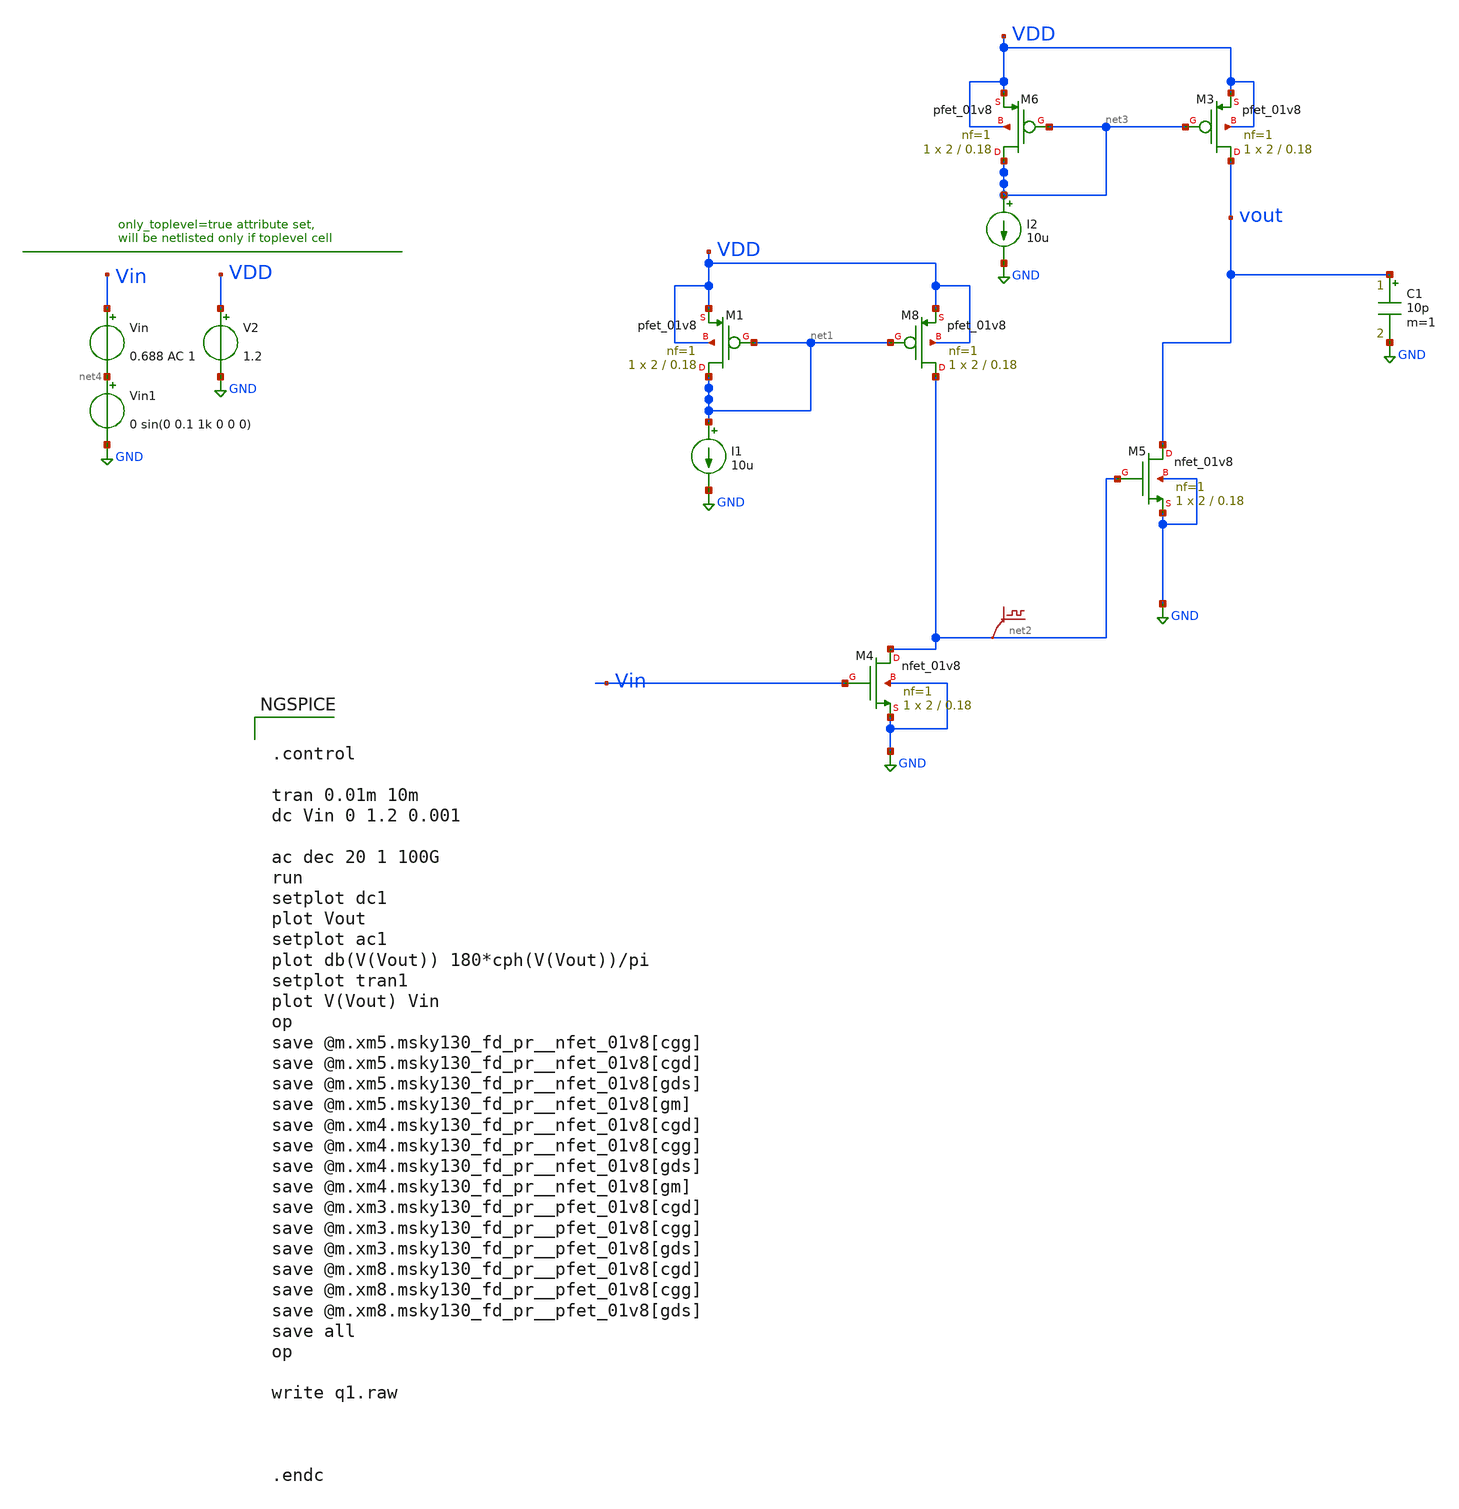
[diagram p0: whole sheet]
** sch_path: q1.sch
**.subckt q1
Vin Vin net4 0.688 AC 1
V2 VDD GND 1.2
XM4 net2 Vin GND GND sky130_fd_pr__nfet_01v8 L=0.18 W=2 nf=1 ad='int((nf+1)/2) * W/nf * 0.29' as='int((nf+2)/2) * W/nf * 0.29'
+ pd='2*int((nf+1)/2) * (W/nf + 0.29)' ps='2*int((nf+2)/2) * (W/nf + 0.29)' nrd='0.29 / W' nrs='0.29 / W'
+ sa=0 sb=0 sd=0 mult=1 m=1
XM5 vout net2 GND GND sky130_fd_pr__nfet_01v8 L=0.18 W=2 nf=1 ad='int((nf+1)/2) * W/nf * 0.29' as='int((nf+2)/2) * W/nf * 0.29'
+ pd='2*int((nf+1)/2) * (W/nf + 0.29)' ps='2*int((nf+2)/2) * (W/nf + 0.29)' nrd='0.29 / W' nrs='0.29 / W'
+ sa=0 sb=0 sd=0 mult=1 m=1
XM8 net2 net1 VDD VDD sky130_fd_pr__pfet_01v8 L=0.18 W=2 nf=1 ad='int((nf+1)/2) * W/nf * 0.29' as='int((nf+2)/2) * W/nf * 0.29'
+ pd='2*int((nf+1)/2) * (W/nf + 0.29)' ps='2*int((nf+2)/2) * (W/nf + 0.29)' nrd='0.29 / W' nrs='0.29 / W'
+ sa=0 sb=0 sd=0 mult=1 m=1
XM1 net1 net1 VDD VDD sky130_fd_pr__pfet_01v8 L=0.18 W=2 nf=1 ad='int((nf+1)/2) * W/nf * 0.29' as='int((nf+2)/2) * W/nf * 0.29'
+ pd='2*int((nf+1)/2) * (W/nf + 0.29)' ps='2*int((nf+2)/2) * (W/nf + 0.29)' nrd='0.29 / W' nrs='0.29 / W'
+ sa=0 sb=0 sd=0 mult=1 m=1
XM3 vout net3 VDD VDD sky130_fd_pr__pfet_01v8 L=0.18 W=2 nf=1 ad='int((nf+1)/2) * W/nf * 0.29' as='int((nf+2)/2) * W/nf * 0.29'
+ pd='2*int((nf+1)/2) * (W/nf + 0.29)' ps='2*int((nf+2)/2) * (W/nf + 0.29)' nrd='0.29 / W' nrs='0.29 / W'
+ sa=0 sb=0 sd=0 mult=1 m=1
XM6 net3 net3 VDD VDD sky130_fd_pr__pfet_01v8 L=0.18 W=2 nf=1 ad='int((nf+1)/2) * W/nf * 0.29' as='int((nf+2)/2) * W/nf * 0.29'
+ pd='2*int((nf+1)/2) * (W/nf + 0.29)' ps='2*int((nf+2)/2) * (W/nf + 0.29)' nrd='0.29 / W' nrs='0.29 / W'
+ sa=0 sb=0 sd=0 mult=1 m=1
I1 net1 GND 10u
I2 net3 GND 10u
C1 vout GND 10p m=1
Vin1 net4 GND 0 sin(0 0.1 1k 0 0 0)
.save v(net2)
**** begin user architecture code

** opencircuitdesign pdks install
.lib $::SKYWATER_MODELS/sky130.lib.spice tt




.control

tran 0.01m 10m
dc Vin 0 1.2 0.001

ac dec 20 1 100G
run
setplot dc1
plot Vout
setplot ac1
plot db(V(Vout)) 180*cph(V(Vout))/pi
setplot tran1
plot V(Vout) Vin
op
save @m.xm5.msky130_fd_pr__nfet_01v8[cgg]
save @m.xm5.msky130_fd_pr__nfet_01v8[cgd]
save @m.xm5.msky130_fd_pr__nfet_01v8[gds]
save @m.xm5.msky130_fd_pr__nfet_01v8[gm]
save @m.xm4.msky130_fd_pr__nfet_01v8[cgd]
save @m.xm4.msky130_fd_pr__nfet_01v8[cgg]
save @m.xm4.msky130_fd_pr__nfet_01v8[gds]
save @m.xm4.msky130_fd_pr__nfet_01v8[gm]
save @m.xm3.msky130_fd_pr__pfet_01v8[cgd]
save @m.xm3.msky130_fd_pr__pfet_01v8[cgg]
save @m.xm3.msky130_fd_pr__pfet_01v8[gds]
save @m.xm8.msky130_fd_pr__pfet_01v8[cgd]
save @m.xm8.msky130_fd_pr__pfet_01v8[cgg]
save @m.xm8.msky130_fd_pr__pfet_01v8[gds]
save all
op

write q1.raw



.endc


**** end user architecture code
**.ends
.GLOBAL GND
.end
